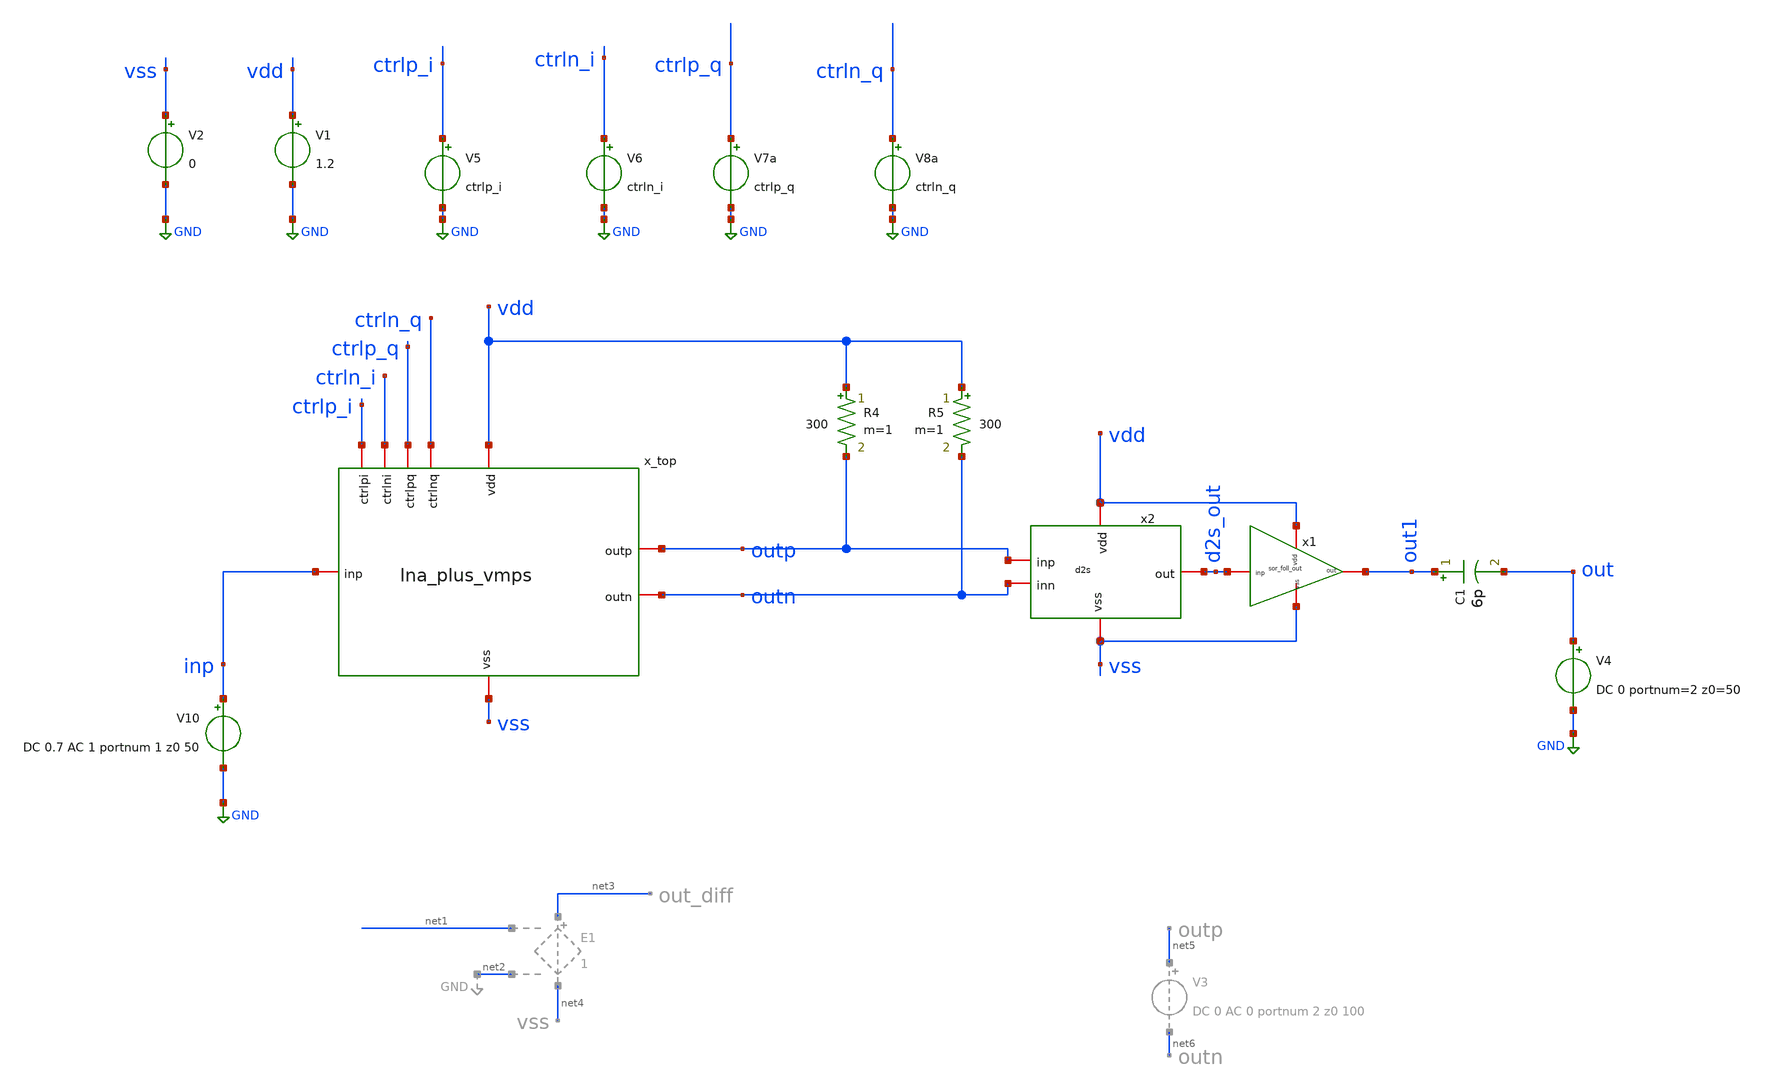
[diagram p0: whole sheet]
** sch_path: LNA7096-main/schematic/xschem/06_integ/lna_plus_vmps_sp.sch
**.subckt lna_plus_vmps_sp
V1 vdd GND 1.2
V5 ctrlp_i GND ctrlp_i
V6 ctrln_i GND ctrln_i
V7a ctrlp_q GND ctrlp_q
V8a ctrln_q GND ctrln_q
V10 inp GND DC 0.7 AC 1 portnum 1 z0 50
R4 vdd outp 300 m=1
R5 vdd outn 300 m=1
x_top vdd ctrlp_i ctrlp_q ctrln_q ctrln_i outp inp outn vss lna_plus_vmps
V2 vss GND 0
x2 vdd d2s_out outp outn vss d2s
V4 out GND DC 0 portnum=2 z0=50
x1 vdd d2s_out out1 vss sor_foll_out
C1 out1 out 6p m=1
**** begin user architecture code

.lib cornerCAP.lib cap_typ
.lib cornerMOSlv.lib mos_tt
.lib cornerMOShv.lib mos_tt
.lib cornerHBT.lib hbt_typ
.lib cornerRES.lib res_typ
.lib cornerDIO.lib dio_tt

.include /home/ic_design_trg/pdk/ihp-sg13g2/libs.ref/sg13g2_stdcell/spice/sg13g2_stdcell.spice



.include /home/ic_design_trg/lna_ihp/xschem/06_integ/simulation/lna_vmps.save
.temp=27


.param ctrlp_i=0.6 ctrln_i=0.9
.param ctrlp_q=0.6 ctrln_q=0.6

.param VDD_val = 1.2
.param CM_rf = 0.6
.param freq = 1.17645G

.control
*  --- 0. Setup and Initialization ---
*  Save all nodes AND the complex S-parameters to conserve them in memory
save all

*  Unset appendwrite initially to ensure we create a fresh file
unset appendwrite

*  --- 1. Define Phase Angle and Control Vectors ---
compose theta_vals start=0 stop=360 step=5.625
let rad_vec = theta_vals * pi / 180

*  Define Constants
let v_cm = 0.6
let v_max = 0.3
let gamma = 1.30

*  --- 2. PRE-DISTORTION SETTING ---
let cos_w = cos(rad_vec)
let sin_w = sin(rad_vec)

*  Use 'gt' and 'lt' to emulate sgn()
let sgn_cos = (cos_w gt 0) - (cos_w lt 0)
let sgn_sin = (sin_w gt 0) - (sin_w lt 0)

*  Apply Power-Law Mapping
let i_corr = sgn_cos * (abs(cos_w)^gamma)
let q_corr = sgn_sin * (abs(sin_w)^gamma)

*  Pre-calculate 4-Quadrant Control Voltages
let pi_p_vec = v_cm + v_max * i_corr
let pi_n_vec = v_cm - v_max * i_corr
let pq_p_vec = v_cm + v_max * q_corr
let pq_n_vec = v_cm - v_max * q_corr

*  --- 3. Initialize Loop ---
let n_runs = length(theta_vals)
let run_idx = 0

*  Capture the start plot (constants) to retrieve vectors later
set start_plot = $curplot

*  Create CSV File Header
*  [UPDATED] Includes calculated voltages, S11, S22, Phase, and Gain
echo theta, V5_cal, V6_cal, V7a_cal, V8a_cal, s11_db, s22_db, phase_deg, gain_db > vmps_sweep.csv

*  --- 4. Execution Loop ---
dowhile run_idx < n_runs
    *  A. Retrieve calculated DC voltages from the start plot
    *  (Syntax corrected to remove stray $ signs)
    let pip_act = {$start_plot}.pi_p_vec[run_idx]
    let pin_act = {$start_plot}.pi_n_vec[run_idx]
    let pqp_act = {$start_plot}.pq_p_vec[run_idx]
    let pqn_act = {$start_plot}.pq_n_vec[run_idx]
    let t_act = {$start_plot}.theta_vals[run_idx]

    *  B. Apply Bias
    alter v5 dc = $&pip_act
    alter v6 dc = $&pin_act
    alter v7a dc = $&pqp_act
    alter v8a dc = $&pqn_act

    *  C. Operating Point Analysis (OP)
    op
    remzerovec

    *  Save OP results to RAW file
    if run_idx = 0
        write lna_plus_vmps_sp.raw all
        set appendwrite
    else
        write lna_plus_vmps_sp.raw all
    end

    *  Free up RAM from the OP evaluation
    destroy $curplot

    *  D. S-Parameter (SP) Simulation
    sp lin 200 0.1G 2.5G

        * ==========================================
        * 1. Schematic Calculations (Port 2)
        * ==========================================
        * Calculate Magnitude (dB) and Phase (Degrees) from S21
        let gain_db_vec = db(S_2_1)
        let phase_deg_vec = cph(S_2_1) * 180 / pi

        * Calculate S11 and S22 in dB
        let s11_db = db(S_1_1)
        let s22_db = db(S_2_2)

        * Measure all values at Fundamental Frequency (1.17645 GHz)
        meas sp gain_db find gain_db_vec at=1.17645e9
        meas sp phase_deg find phase_deg_vec at=1.17645e9
        meas sp s11_val find s11_db at=1.17645e9
        meas sp s22_val find s22_db at=1.17645e9

        * ==========================================
        * 2. Write Results
        * ==========================================
        * [UPDATED] Writes the exact mathematically calculated targets alongside S-Parameters
        echo $&t_act, $&pip_act, $&pin_act, $&pqp_act, $&pqn_act, $&s11_val, $&s22_val, $&phase_deg,
+ $&gain_db >> vmps_sweep.csv

        * Save SP results to RAW file (appending sequentially)
        write lna_plus_vmps_sp.raw S_1_1 S_2_1 S_1_2 S_2_2 gain_db_vec phase_deg_vec s11_db s22_db

        * Free up RAM from the SP evaluation before the next loop
        destroy $curplot

    let run_idx = run_idx + 1
end
.endc



**** end user architecture code
**.ends
.GLOBAL GND
.end
